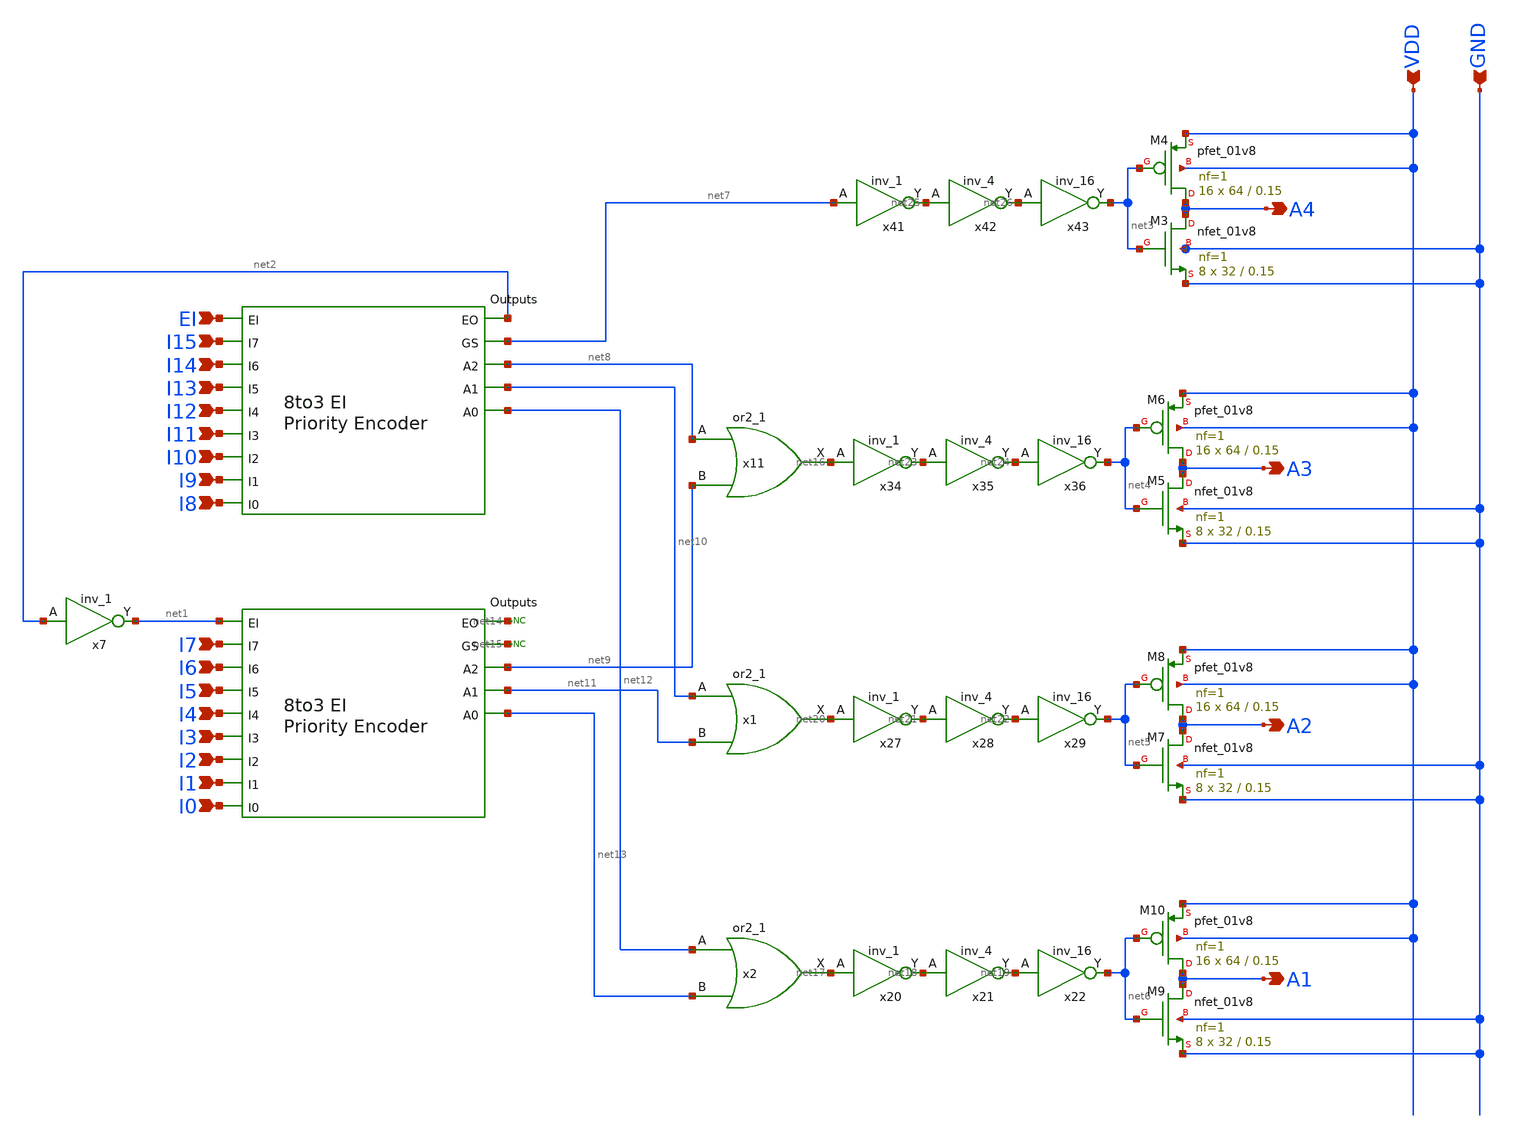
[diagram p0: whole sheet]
** sch_path: PriorityEncoder/xschem/16to4_PriorityEncoder_v0p0p1.sch
.lib $::SKYWATER_MODELS/sky130.lib.spice tt
.include $::SKYWATER_STDCELLS/sky130_fd_sc_hd.spice

**.subckt 16to4_PriorityEncoder_v0p0p1 I14 I13 I12 I11 I10 I9 I8 I7 I6 I5 I4 I3 I2 I1 I0 A4 A3 A2 A1
*+ VDD GND I15 EI
*.ipin I14
*.ipin I13
*.ipin I12
*.ipin I11
*.ipin I10
*.ipin I9
*.ipin I8
*.ipin I7
*.ipin I6
*.ipin I5
*.ipin I4
*.ipin I3
*.ipin I2
*.ipin I1
*.ipin I0
*.opin A4
*.opin A3
*.opin A2
*.opin A1
*.ipin VDD
*.ipin GND
*.ipin I15
*.ipin EI
x3 I9 I13 I11 I8 I10 I14 I15 I12 net2 net7 net8 net10 net12 EI 8to3_Priority_Encoder_v0p2p0
x4 I1 I5 I3 I0 I2 I6 I7 I4 net14 net15 net9 net11 net13 net1 8to3_Priority_Encoder_v0p2p0
x11 net8 net9 GND GND VDD VDD net16 sky130_fd_sc_hd__or2_1
x20 net17 GND GND VDD VDD net18 sky130_fd_sc_hd__inv_1
x21 net18 GND GND VDD VDD net19 sky130_fd_sc_hd__inv_4
x22 net19 GND GND VDD VDD net6 sky130_fd_sc_hd__inv_16
x27 net20 GND GND VDD VDD net21 sky130_fd_sc_hd__inv_1
x28 net21 GND GND VDD VDD net22 sky130_fd_sc_hd__inv_4
x29 net22 GND GND VDD VDD net5 sky130_fd_sc_hd__inv_16
x34 net16 GND GND VDD VDD net23 sky130_fd_sc_hd__inv_1
x35 net23 GND GND VDD VDD net24 sky130_fd_sc_hd__inv_4
x36 net24 GND GND VDD VDD net4 sky130_fd_sc_hd__inv_16
x41 net7 GND GND VDD VDD net25 sky130_fd_sc_hd__inv_1
x42 net25 GND GND VDD VDD net26 sky130_fd_sc_hd__inv_4
x43 net26 GND GND VDD VDD net3 sky130_fd_sc_hd__inv_16
XM3 A4 net3 GND GND sky130_fd_pr__nfet_01v8 L=0.15 W=32 nf=1 ad='int((nf+1)/2) * W/nf * 0.29' as='int((nf+2)/2) * W/nf * 0.29'
+ pd='2*int((nf+1)/2) * (W/nf + 0.29)' ps='2*int((nf+2)/2) * (W/nf + 0.29)' nrd='0.29 / W' nrs='0.29 / W'
+ sa=0 sb=0 sd=0 mult=8 m=8
XM4 A4 net3 VDD VDD sky130_fd_pr__pfet_01v8 L=0.15 W=64 nf=1 ad='int((nf+1)/2) * W/nf * 0.29' as='int((nf+2)/2) * W/nf * 0.29'
+ pd='2*int((nf+1)/2) * (W/nf + 0.29)' ps='2*int((nf+2)/2) * (W/nf + 0.29)' nrd='0.29 / W' nrs='0.29 / W'
+ sa=0 sb=0 sd=0 mult=16 m=16
XM5 A3 net4 GND GND sky130_fd_pr__nfet_01v8 L=0.15 W=32 nf=1 ad='int((nf+1)/2) * W/nf * 0.29' as='int((nf+2)/2) * W/nf * 0.29'
+ pd='2*int((nf+1)/2) * (W/nf + 0.29)' ps='2*int((nf+2)/2) * (W/nf + 0.29)' nrd='0.29 / W' nrs='0.29 / W'
+ sa=0 sb=0 sd=0 mult=8 m=8
XM6 A3 net4 VDD VDD sky130_fd_pr__pfet_01v8 L=0.15 W=64 nf=1 ad='int((nf+1)/2) * W/nf * 0.29' as='int((nf+2)/2) * W/nf * 0.29'
+ pd='2*int((nf+1)/2) * (W/nf + 0.29)' ps='2*int((nf+2)/2) * (W/nf + 0.29)' nrd='0.29 / W' nrs='0.29 / W'
+ sa=0 sb=0 sd=0 mult=16 m=16
XM7 A2 net5 GND GND sky130_fd_pr__nfet_01v8 L=0.15 W=32 nf=1 ad='int((nf+1)/2) * W/nf * 0.29' as='int((nf+2)/2) * W/nf * 0.29'
+ pd='2*int((nf+1)/2) * (W/nf + 0.29)' ps='2*int((nf+2)/2) * (W/nf + 0.29)' nrd='0.29 / W' nrs='0.29 / W'
+ sa=0 sb=0 sd=0 mult=8 m=8
XM8 A2 net5 VDD VDD sky130_fd_pr__pfet_01v8 L=0.15 W=64 nf=1 ad='int((nf+1)/2) * W/nf * 0.29' as='int((nf+2)/2) * W/nf * 0.29'
+ pd='2*int((nf+1)/2) * (W/nf + 0.29)' ps='2*int((nf+2)/2) * (W/nf + 0.29)' nrd='0.29 / W' nrs='0.29 / W'
+ sa=0 sb=0 sd=0 mult=16 m=16
XM9 A1 net6 GND GND sky130_fd_pr__nfet_01v8 L=0.15 W=32 nf=1 ad='int((nf+1)/2) * W/nf * 0.29' as='int((nf+2)/2) * W/nf * 0.29'
+ pd='2*int((nf+1)/2) * (W/nf + 0.29)' ps='2*int((nf+2)/2) * (W/nf + 0.29)' nrd='0.29 / W' nrs='0.29 / W'
+ sa=0 sb=0 sd=0 mult=8 m=8
XM10 A1 net6 VDD VDD sky130_fd_pr__pfet_01v8 L=0.15 W=64 nf=1 ad='int((nf+1)/2) * W/nf * 0.29' as='int((nf+2)/2) * W/nf * 0.29'
+ pd='2*int((nf+1)/2) * (W/nf + 0.29)' ps='2*int((nf+2)/2) * (W/nf + 0.29)' nrd='0.29 / W' nrs='0.29 / W'
+ sa=0 sb=0 sd=0 mult=16 m=16
x7 net2 GND GND VDD VDD net1 sky130_fd_sc_hd__inv_1
x1 net10 net11 GND GND VDD VDD net20 sky130_fd_sc_hd__or2_1
x2 net12 net13 GND GND VDD VDD net17 sky130_fd_sc_hd__or2_1
* noconn #net14
* noconn #net15
**.ends
.end
